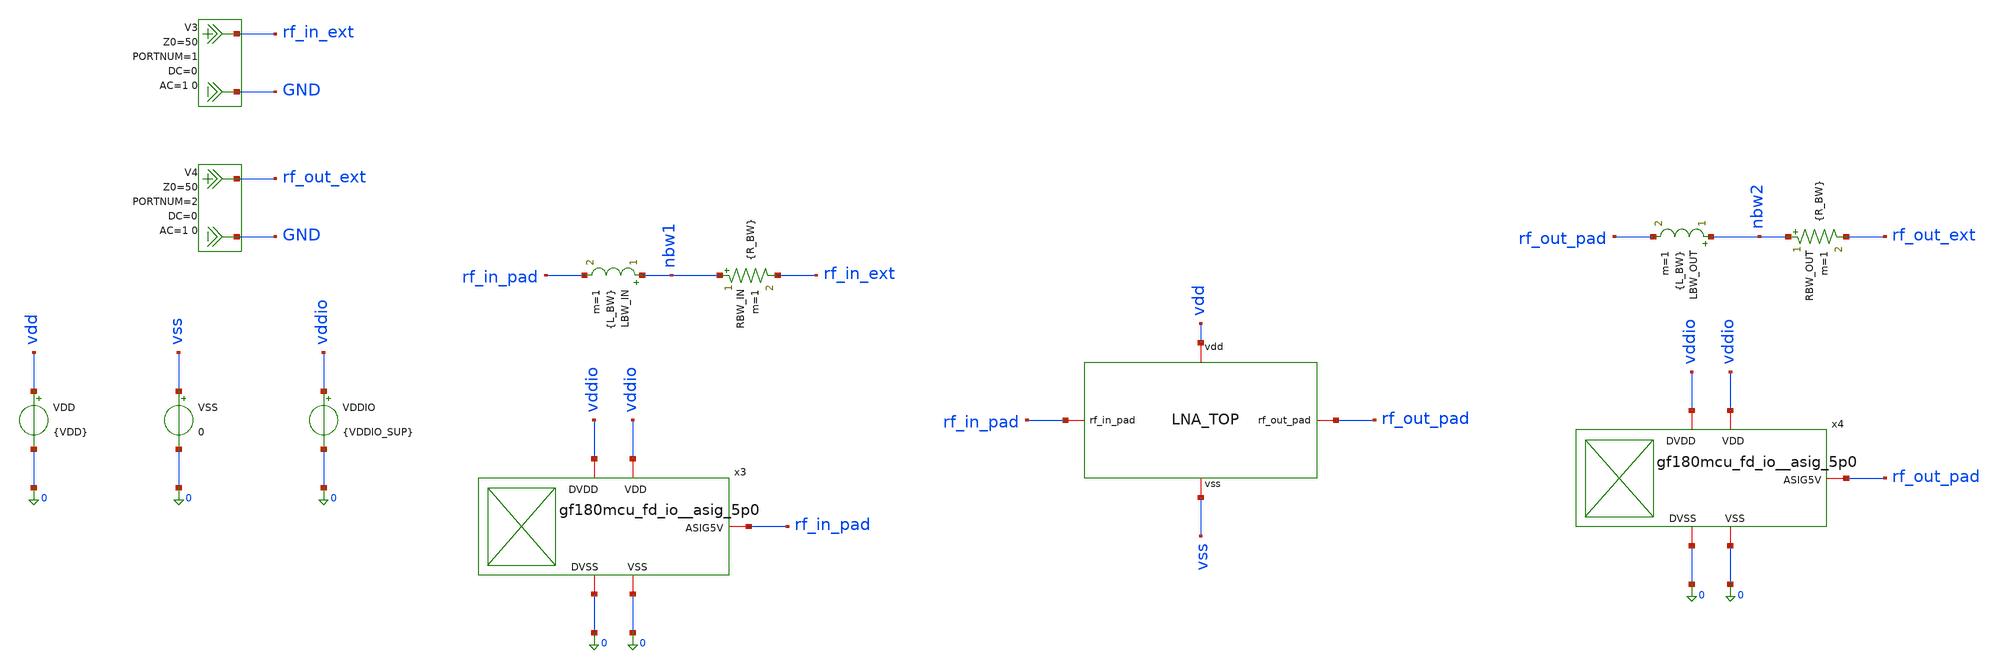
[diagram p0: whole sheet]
** sch_path: xschem/lna_v2/lna_top_tb.sch
**.subckt lna_top_tb
x3 rf_in_pad vddio 0 vddio 0 gf180mcu_fd_io__asig_5p0
x4 rf_out_pad vddio 0 vddio 0 gf180mcu_fd_io__asig_5p0
LBW_IN nbw1 rf_in_pad {L_BW} m=1
RBW_IN nbw1 rf_in_ext {R_BW} m=1
LBW_OUT nbw2 rf_out_pad {L_BW} m=1
RBW_OUT nbw2 rf_out_ext {R_BW} m=1
VDD vdd 0 {VDD}
VSS vss 0 0
VDDIO vddio 0 {VDDIO_SUP}
V3 rf_in_ext GND DC 0 AC 1 0 portnum 1 z0 50
V4 rf_out_ext GND DC 0 AC 1 0 portnum 2 z0 50
x1 vdd rf_in_pad rf_out_pad vss lna_top
**** begin user architecture code

.include ${::180MCU_MODELS}/design.ngspice
.lib ${::180MCU_MODELS}/sm141064.ngspice typical
.lib ${::180MCU_MODELS}/sm141064.ngspice res_typical
.lib ${::180MCU_MODELS}/sm141064.ngspice moscap_typical
.lib ${::180MCU_MODELS}/sm141064.ngspice diode_typical
.lib ${::180MCU_MODELS}/sm141064.ngspice bjt_typical
.lib ${::180MCU_MODELS}/sm141064.ngspice mimcap_typical



* extracted RC pad network (magic flat RC extraction, nominal); high-C corner: pad_rcxhrhc.spice
*.include /home/arjun/.xschem/simulations/lna_test/optimization/pad_audit/pad_rcxnom.spice
.include /home/arjun/eda/projects/The-Silent-Owl-GF180MCU-WB-LNA/analog_pad_sp_paramerters/spice_files/extracted_gf180mcu_fd_io__asig_5p0_manually_scaled.spice




.param VDD=5.0 VDDIO_SUP=5.0 L_BW=3n R_BW=0.2
.temp 27





.control

set noaskquit
set wr_singlescale
set wr_vecnames
set numdgt=10

option klu
set num_threads=6

let spec_gain_min_db = 10
let spec_s11_max_db  = -10
let spec_s22_max_db  = -10
let spec_nf_max_db   = 2.0
let spec_mu_min      = 1.0
let spec_k_min       = 1.0
let spec_delta_max   = 1.0
let spec_pdc_max_mw  = 130

let f_target_lo = 2.3e9
let f_target    = 2.4e9
let f_target_hi = 2.5e9



echo ============================================================ > lna_final_report.txt
echo GF180MCU_WIDEBAND_LNA_FINAL_CHARACTERIZATION >> lna_final_report.txt
echo ============================================================ >> lna_final_report.txt
echo TARGET_CENTER_HZ 2.400e9 >> lna_final_report.txt
echo TARGET_BAND_HZ 2.300e9 2.500e9 >> lna_final_report.txt
echo PORT_REFERENCE_OHM 50 >> lna_final_report.txt
echo VDD_NOMINAL_V 5.0 >> lna_final_report.txt
echo HIERARCHY TB_X1_LNA_TOP_X1_LNA_CORE >> lna_final_report.txt
echo S_PARAMETER_REFERENCE_PLANE EXTERNAL_PORTS_INCLUDING_PADS_BONDWIRES >> lna_final_report.txt

echo SPEC_GAIN_MIN_DB $&spec_gain_min_db >> lna_final_report.txt
echo SPEC_S11_MAX_DB $&spec_s11_max_db >> lna_final_report.txt
echo SPEC_S22_MAX_DB $&spec_s22_max_db >> lna_final_report.txt
echo SPEC_NF_MAX_DB $&spec_nf_max_db >> lna_final_report.txt
echo SPEC_PDC_MAX_MW $&spec_pdc_max_mw >> lna_final_report.txt
echo ============================================================ >> lna_final_report.txt


op


let pdc_lna_mw = 1e3*abs(i(VDD))*v(vdd)
let pdc_io_mw  = 1e3*abs(i(VDDIO))*v(vddio)
let pdc_total_mw = pdc_lna_mw+pdc_io_mw

let idd_lna = abs(i(VDD))
let idd_io  = abs(i(VDDIO))

set op_pdc_lna   = $&pdc_lna_mw
set op_pdc_io    = $&pdc_io_mw
set op_pdc_total = $&pdc_total_mw
set op_idd_lna   = $&idd_lna
set op_idd_io    = $&idd_io



let vbias_cg_op   = v(x1.vbias_cg)
let vbias_cs_op   = v(x1.vbias_cs)
let vbias_csc_op  = v(x1.vbias_csc)
let vbias_cas_op  = v(x1.vbias_cas)
let vbias_casc_op = v(x1.vbias_casc)

set op_vbias_cg   = $&vbias_cg_op
set op_vbias_cs   = $&vbias_cs_op
set op_vbias_csc  = $&vbias_csc_op
set op_vbias_cas  = $&vbias_cas_op
set op_vbias_casc = $&vbias_casc_op


let vm2_op     = v(x1.x1.vm2)
let gcg_op     = v(x1.x1.g_cg)

let gcs_op     = v(x1.x1.g_cs)
let xm1s_op    = v(x1.x1.xm1_s)
let vm1_op     = v(x1.x1.vm1)

let gcsc_op    = v(x1.x1.g_csc)
let xm9s_op    = v(x1.x1.xm9_s)
let xm9d_op    = v(x1.x1.xm9_d)

let vx_op      = v(x1.x1.vx)

let vbp3_op    = v(x1.x1.vbp3)
let ngp3_op    = v(x1.x1.ngp3)
let np3d_op    = v(x1.x1.np3d)
let noutc_op   = v(x1.x1.nout_c)

set op_vm2   = $&vm2_op
set op_gcg   = $&gcg_op
set op_gcs   = $&gcs_op
set op_xm1s  = $&xm1s_op
set op_vm1   = $&vm1_op
set op_gcsc  = $&gcsc_op
set op_xm9s  = $&xm9s_op
set op_xm9d  = $&xm9d_op
set op_vx    = $&vx_op
set op_vbp3  = $&vbp3_op
set op_ngp3  = $&ngp3_op
set op_np3d  = $&np3d_op
set op_noutc = $&noutc_op

let id1    = abs(@m.x1.x1.xm1.m0[id])
let gm1    = abs(@m.x1.x1.xm1.m0[gm])
let gmb1   = abs(@m.x1.x1.xm1.m0[gmbs])
let gds1   = abs(@m.x1.x1.xm1.m0[gds])

let vgs1   = @m.x1.x1.xm1.m0[vgs]
let vds1   = @m.x1.x1.xm1.m0[vds]
let vth1   = @m.x1.x1.xm1.m0[vth]
let vdsat1 = @m.x1.x1.xm1.m0[vdsat]

let gmid1  = gm1/(id1+1e-30)
let ro1    = 1/(gds1+1e-30)
let sat1   = abs(vds1)-abs(vdsat1)

let id2    = abs(@m.x1.x1.xm2.m0[id])
let gm2    = abs(@m.x1.x1.xm2.m0[gm])
let gmb2   = abs(@m.x1.x1.xm2.m0[gmbs])
let gds2   = abs(@m.x1.x1.xm2.m0[gds])

let vgs2   = @m.x1.x1.xm2.m0[vgs]
let vds2   = @m.x1.x1.xm2.m0[vds]
let vth2   = @m.x1.x1.xm2.m0[vth]
let vdsat2 = @m.x1.x1.xm2.m0[vdsat]

let gmid2  = gm2/(id2+1e-30)
let ro2    = 1/(gds2+1e-30)
let sat2   = abs(vds2)-abs(vdsat2)

let id4    = abs(@m.x1.x1.xm4.m0[id])
let gm4    = abs(@m.x1.x1.xm4.m0[gm])
let gmb4   = abs(@m.x1.x1.xm4.m0[gmbs])
let gds4   = abs(@m.x1.x1.xm4.m0[gds])

let vgs4   = @m.x1.x1.xm4.m0[vgs]
let vds4   = @m.x1.x1.xm4.m0[vds]
let vth4   = @m.x1.x1.xm4.m0[vth]
let vdsat4 = @m.x1.x1.xm4.m0[vdsat]

let gmid4  = gm4/(id4+1e-30)
let ro4    = 1/(gds4+1e-30)
let sat4   = abs(vds4)-abs(vdsat4)

let id9    = abs(@m.x1.x1.xm9.m0[id])
let gm9    = abs(@m.x1.x1.xm9.m0[gm])
let gmb9   = abs(@m.x1.x1.xm9.m0[gmbs])
let gds9   = abs(@m.x1.x1.xm9.m0[gds])

let vgs9   = @m.x1.x1.xm9.m0[vgs]
let vds9   = @m.x1.x1.xm9.m0[vds]
let vth9   = @m.x1.x1.xm9.m0[vth]
let vdsat9 = @m.x1.x1.xm9.m0[vdsat]

let gmid9  = gm9/(id9+1e-30)
let ro9    = 1/(gds9+1e-30)
let sat9   = abs(vds9)-abs(vdsat9)

let id7    = abs(@m.x1.x1.xm7.m0[id])
let gm7    = abs(@m.x1.x1.xm7.m0[gm])
let gmb7   = abs(@m.x1.x1.xm7.m0[gmbs])
let gds7   = abs(@m.x1.x1.xm7.m0[gds])

let vgs7   = @m.x1.x1.xm7.m0[vgs]
let vds7   = @m.x1.x1.xm7.m0[vds]
let vth7   = @m.x1.x1.xm7.m0[vth]
let vdsat7 = @m.x1.x1.xm7.m0[vdsat]

let gmid7  = gm7/(id7+1e-30)
let ro7    = 1/(gds7+1e-30)
let sat7   = abs(vds7)-abs(vdsat7)

let idp3    = abs(@m.x1.x1.xmp3.m0[id])
let gmp3    = abs(@m.x1.x1.xmp3.m0[gm])
let gmbp3   = abs(@m.x1.x1.xmp3.m0[gmbs])
let gdsp3   = abs(@m.x1.x1.xmp3.m0[gds])

let vgsp3   = @m.x1.x1.xmp3.m0[vgs]
let vdsp3   = @m.x1.x1.xmp3.m0[vds]
let vthp3   = @m.x1.x1.xmp3.m0[vth]
let vdsatp3 = @m.x1.x1.xmp3.m0[vdsat]

let gmidp3  = gmp3/(idp3+1e-30)
let rop3    = 1/(gdsp3+1e-30)
let satp3   = abs(vdsp3)-abs(vdsatp3)


let idbp3    = abs(@m.x1.x1.xbp3.m0[id])
let gmbp3x   = abs(@m.x1.x1.xbp3.m0[gm])
let gdsbp3   = abs(@m.x1.x1.xbp3.m0[gds])

let vgsbp3   = @m.x1.x1.xbp3.m0[vgs]
let vdsbp3   = @m.x1.x1.xbp3.m0[vds]
let vthbp3   = @m.x1.x1.xbp3.m0[vth]
let vdsatbp3 = @m.x1.x1.xbp3.m0[vdsat]

let gmidbp3 = gmbp3x/(idbp3+1e-30)
let robp3   = 1/(gdsbp3+1e-30)
let satbp3  = abs(vdsbp3)-abs(vdsatbp3)

set op_id1=$&id1
set op_gm1=$&gm1
set op_gmid1=$&gmid1
set op_ro1=$&ro1
set op_vgs1=$&vgs1
set op_vds1=$&vds1
set op_vdsat1=$&vdsat1
set op_sat1=$&sat1

set op_id2=$&id2
set op_gm2=$&gm2
set op_gmid2=$&gmid2
set op_ro2=$&ro2
set op_vgs2=$&vgs2
set op_vds2=$&vds2
set op_vdsat2=$&vdsat2
set op_sat2=$&sat2

set op_id4=$&id4
set op_gm4=$&gm4
set op_gmid4=$&gmid4
set op_ro4=$&ro4
set op_vgs4=$&vgs4
set op_vds4=$&vds4
set op_vdsat4=$&vdsat4
set op_sat4=$&sat4

set op_id9=$&id9
set op_gm9=$&gm9
set op_gmid9=$&gmid9
set op_ro9=$&ro9
set op_vgs9=$&vgs9
set op_vds9=$&vds9
set op_vdsat9=$&vdsat9
set op_sat9=$&sat9

set op_id7=$&id7
set op_gm7=$&gm7
set op_gmid7=$&gmid7
set op_ro7=$&ro7
set op_vgs7=$&vgs7
set op_vds7=$&vds7
set op_vdsat7=$&vdsat7
set op_sat7=$&sat7

set op_idp3=$&idp3
set op_gmp3=$&gmp3
set op_gmidp3=$&gmidp3
set op_rop3=$&rop3
set op_vgsp3=$&vgsp3
set op_vdsp3=$&vdsp3
set op_vdsatp3=$&vdsatp3
set op_satp3=$&satp3

set op_idbp3=$&idbp3
set op_gmbp3=$&gmbp3x
set op_gmidbp3=$&gmidbp3
set op_robp3=$&robp3
set op_vgsbp3=$&vgsbp3
set op_vdsbp3=$&vdsbp3
set op_vdsatbp3=$&vdsatbp3
set op_satbp3=$&satbp3


* ============================================================================
* WRITE DC REPORT
* ============================================================================

echo ============================================================ >> lna_final_report.txt
echo DC_POWER >> lna_final_report.txt
echo ============================================================ >> lna_final_report.txt

echo LNA_TOP_POWER_MW $op_pdc_lna >> lna_final_report.txt
echo IO_PAD_POWER_MW $op_pdc_io >> lna_final_report.txt
echo TOTAL_POWER_MW $op_pdc_total >> lna_final_report.txt
echo LNA_TOP_CURRENT_A $op_idd_lna >> lna_final_report.txt
echo IO_CURRENT_A $op_idd_io >> lna_final_report.txt


echo ============================================================ >> lna_final_report.txt
echo BIAS_VOLTAGES >> lna_final_report.txt
echo ============================================================ >> lna_final_report.txt

echo VBIAS_CG_V $op_vbias_cg >> lna_final_report.txt
echo VBIAS_CS_V $op_vbias_cs >> lna_final_report.txt
echo VBIAS_CSC_V $op_vbias_csc >> lna_final_report.txt
echo VBIAS_CAS_V $op_vbias_cas >> lna_final_report.txt
echo VBIAS_CASC_V $op_vbias_casc >> lna_final_report.txt


echo ============================================================ >> lna_final_report.txt
echo CORE_DC_NODE_VOLTAGES >> lna_final_report.txt
echo ============================================================ >> lna_final_report.txt

echo VM2_V $op_vm2 >> lna_final_report.txt
echo G_CG_V $op_gcg >> lna_final_report.txt

echo G_CS_V $op_gcs >> lna_final_report.txt
echo XM1_SOURCE_V $op_xm1s >> lna_final_report.txt
echo VM1_V $op_vm1 >> lna_final_report.txt

echo G_CSC_V $op_gcsc >> lna_final_report.txt
echo XM9_SOURCE_V $op_xm9s >> lna_final_report.txt
echo XM9_DRAIN_V $op_xm9d >> lna_final_report.txt

echo VX_V $op_vx >> lna_final_report.txt

echo VBP3_V $op_vbp3 >> lna_final_report.txt
echo NGP3_V $op_ngp3 >> lna_final_report.txt
echo NP3D_V $op_np3d >> lna_final_report.txt
echo NOUT_C_V $op_noutc >> lna_final_report.txt


echo ============================================================ >> lna_final_report.txt
echo TRANSISTOR_OPERATING_POINTS >> lna_final_report.txt
echo FIELDS ID_A GM_S GMID_1_PER_V RO_OHM VGS_V VDS_V VDSAT_V SAT_MARGIN_V >> lna_final_report.txt
echo ============================================================ >> lna_final_report.txt

echo XM1_MAIN_CS ID $op_id1 GM $op_gm1 GMID $op_gmid1 RO $op_ro1 VGS $op_vgs1 VDS $op_vds1 VDSAT
+ $op_vdsat1 SAT_MARGIN $op_sat1 >> lna_final_report.txt

echo XM2_INPUT_CG ID $op_id2 GM $op_gm2 GMID $op_gmid2 RO $op_ro2 VGS $op_vgs2 VDS $op_vds2 VDSAT
+ $op_vdsat2 SAT_MARGIN $op_sat2 >> lna_final_report.txt

echo XM4_MAIN_CASCODE ID $op_id4 GM $op_gm4 GMID $op_gmid4 RO $op_ro4 VGS $op_vgs4 VDS $op_vds4
+ VDSAT $op_vdsat4 SAT_MARGIN $op_sat4 >> lna_final_report.txt

echo XM9_CANCELLATION_CS ID $op_id9 GM $op_gm9 GMID $op_gmid9 RO $op_ro9 VGS $op_vgs9 VDS $op_vds9
+ VDSAT $op_vdsat9 SAT_MARGIN $op_sat9 >> lna_final_report.txt

echo XM7_CANCELLATION_CASCODE ID $op_id7 GM $op_gm7 GMID $op_gmid7 RO $op_ro7 VGS $op_vgs7 VDS
+ $op_vds7 VDSAT $op_vdsat7 SAT_MARGIN $op_sat7 >> lna_final_report.txt

echo XMP3_OUTPUT_PMOS ID $op_idp3 GM $op_gmp3 GMID $op_gmidp3 RO $op_rop3 VGS $op_vgsp3 VDS
+ $op_vdsp3 VDSAT $op_vdsatp3 SAT_MARGIN $op_satp3 >> lna_final_report.txt

echo XBP3_PMOS_BIAS ID $op_idbp3 GM $op_gmbp3 GMID $op_gmidbp3 RO $op_robp3 VGS $op_vgsbp3 VDS
+ $op_vdsbp3 VDSAT $op_vdsatbp3 SAT_MARGIN $op_satbp3 >> lna_final_report.txt


* ============================================================================
* POWER SPECIFICATION CHECK
* ============================================================================

echo ============================================================ >> lna_final_report.txt
echo DC_SPEC_CHECK >> lna_final_report.txt

if pdc_lna_mw <= spec_pdc_max_mw
    echo POWER PASS >> lna_final_report.txt
else
    echo POWER FAIL >> lna_final_report.txt
end


* We no longer require OP plot vectors after storing scalar values.
destroy $curplot



* ============================================================================
* 2. BROADBAND S-PARAMETER + NOISE ANALYSIS
*
* SP noise flag = 1.
*
* 7000 linearly spaced points:
*   1 MHz --> 7 GHz
*
* This gives roughly 1 MHz resolution, including the complete 2.3-2.5 GHz
* target band.
* ============================================================================

reset
sp lin 7000 1Meg 7Gig 1

set rfplot=$curplot

let fghz=frequency/1e9


* ============================================================================
* S PARAMETERS
* ============================================================================

let s11db=db(s_1_1)
let s21db=db(s_2_1)
let s12db=db(s_1_2)
let s22db=db(s_2_2)

let a11=mag(s_1_1)
let a21=mag(s_2_1)
let a12=mag(s_1_2)
let a22=mag(s_2_2)


* ============================================================================
* NOISE
* ============================================================================

let nfdb=real(NF)
let nfmin_db=real(NFmin)


* ============================================================================
* STABILITY FROM S-PARAMETERS
* ============================================================================

let delta=s_1_1*s_2_2-s_1_2*s_2_1
let delta_mag=mag(delta)

let kval=(1-a11*a11-a22*a22+delta_mag*delta_mag)/(2*a12*a21+1e-30)

let mu=(1-a11*a11)/(mag(s_2_2-delta*conj(s_1_1))+mag(s_1_2*s_2_1)+1e-30)

let mup=(1-a22*a22)/(mag(s_1_1-delta*conj(s_2_2))+mag(s_1_2*s_2_1)+1e-30)


* ============================================================================
* INPUT / OUTPUT IMPEDANCE
* ============================================================================

let zin=50*(1+s_1_1)/(1-s_1_1)
let zout=50*(1+s_2_2)/(1-s_2_2)

let zin_re=real(zin)
let zin_im=imag(zin)

let zout_re=real(zout)
let zout_im=imag(zout)


* ============================================================================
* INPUT / OUTPUT VSWR
* ============================================================================

let vswr_in=(1+a11)/(1-a11+1e-30)
let vswr_out=(1+a22)/(1-a22+1e-30)


* ============================================================================
* FIND 2.3 / 2.4 / 2.5 GHz INDICES
* ============================================================================

let npts=length(frequency)

let ilo=0
let icenter=0
let ihi=0

let errlo=abs(frequency[0]-2.3e9)
let errcenter=abs(frequency[0]-2.4e9)
let errhi=abs(frequency[0]-2.5e9)

let ii=1

while ii < npts

    let newerr=abs(frequency[ii]-2.3e9)

    if newerr < errlo
        let errlo=newerr
        let ilo=ii
    end

    let newerr=abs(frequency[ii]-2.4e9)

    if newerr < errcenter
        let errcenter=newerr
        let icenter=ii
    end

    let newerr=abs(frequency[ii]-2.5e9)

    if newerr < errhi
        let errhi=newerr
        let ihi=ii
    end

    let ii=ii+1

end


* ============================================================================
* VALUES AT 2.4 GHz
* ============================================================================

let fc=frequency[icenter]

let s11c=s11db[icenter]
let s21c=s21db[icenter]
let s12c=s12db[icenter]
let s22c=s22db[icenter]

let nfc=nfdb[icenter]
let nfminc=nfmin_db[icenter]

let kc=kval[icenter]
let muc=mu[icenter]
let mupc=mup[icenter]
let deltac=delta_mag[icenter]

let zinrc=zin_re[icenter]
let zinic=zin_im[icenter]

let zoutrc=zout_re[icenter]
let zoutic=zout_im[icenter]

let vswrinc=vswr_in[icenter]
let vswroutc=vswr_out[icenter]


* ============================================================================
* TARGET-BAND MIN / MAX INITIALIZATION
* ============================================================================

let s11min=s11db[ilo]
let s11max=s11db[ilo]

let s21min=s21db[ilo]
let s21max=s21db[ilo]

let s12min=s12db[ilo]
let s12max=s12db[ilo]

let s22min=s22db[ilo]
let s22max=s22db[ilo]

let nfbandmin=nfdb[ilo]
let nfbandmax=nfdb[ilo]

let nfminpar_min=nfmin_db[ilo]
let nfminpar_max=nfmin_db[ilo]

let kbandmin=kval[ilo]
let mubandmin=mu[ilo]
let mupbandmin=mup[ilo]

let deltabandmax=delta_mag[ilo]

let zinremin=zin_re[ilo]
let zinremax=zin_re[ilo]

let vswrinmax=vswr_in[ilo]
let vswroutmax=vswr_out[ilo]


* indices
let s11max_i=ilo
let s21min_i=ilo
let s21max_i=ilo
let s22max_i=ilo

let nfmax_i=ilo
let nfmin_i=ilo

let kmin_i=ilo
let mumin_i=ilo
let mupmin_i=ilo
let deltamax_i=ilo

let vswrinmax_i=ilo
let vswroutmax_i=ilo


* ============================================================================
* TARGET-BAND SEARCH
* ============================================================================

let ii=ilo

while ii <= ihi

    if s11db[ii] < s11min
        let s11min=s11db[ii]
    end

    if s11db[ii] > s11max
        let s11max=s11db[ii]
        let s11max_i=ii
    end


    if s21db[ii] < s21min
        let s21min=s21db[ii]
        let s21min_i=ii
    end

    if s21db[ii] > s21max
        let s21max=s21db[ii]
        let s21max_i=ii
    end


    if s12db[ii] < s12min
        let s12min=s12db[ii]
    end

    if s12db[ii] > s12max
        let s12max=s12db[ii]
    end


    if s22db[ii] < s22min
        let s22min=s22db[ii]
    end

    if s22db[ii] > s22max
        let s22max=s22db[ii]
        let s22max_i=ii
    end


    if nfdb[ii] < nfbandmin
        let nfbandmin=nfdb[ii]
        let nfmin_i=ii
    end

    if nfdb[ii] > nfbandmax
        let nfbandmax=nfdb[ii]
        let nfmax_i=ii
    end


    if nfmin_db[ii] < nfminpar_min
        let nfminpar_min=nfmin_db[ii]
    end

    if nfmin_db[ii] > nfminpar_max
        let nfminpar_max=nfmin_db[ii]
    end


    if kval[ii] < kbandmin
        let kbandmin=kval[ii]
        let kmin_i=ii
    end

    if mu[ii] < mubandmin
        let mubandmin=mu[ii]
        let mumin_i=ii
    end

    if mup[ii] < mupbandmin
        let mupbandmin=mup[ii]
        let mupmin_i=ii
    end

    if delta_mag[ii] > deltabandmax
        let deltabandmax=delta_mag[ii]
        let deltamax_i=ii
    end


    if vswr_in[ii] > vswrinmax
        let vswrinmax=vswr_in[ii]
        let vswrinmax_i=ii
    end

    if vswr_out[ii] > vswroutmax
        let vswroutmax=vswr_out[ii]
        let vswroutmax_i=ii
    end

    let ii=ii+1

end


* ============================================================================
* DERIVED BAND METRICS
* ============================================================================

let gain_ripple=s21max-s21min

let s11worst_f=frequency[s11max_i]
let s21min_f=frequency[s21min_i]
let s21max_f=frequency[s21max_i]
let s22worst_f=frequency[s22max_i]

let nfmin_f=frequency[nfmin_i]
let nfmax_f=frequency[nfmax_i]

let kmin_f=frequency[kmin_i]
let mumin_f=frequency[mumin_i]
let mupmin_f=frequency[mupmin_i]
let deltamax_f=frequency[deltamax_i]

let vswrinmax_f=frequency[vswrinmax_i]
let vswroutmax_f=frequency[vswroutmax_i]


* ============================================================================
* BROADBAND GAIN PEAK
* ============================================================================

let imax=0
let gainmax=s21db[0]

let ii=1

while ii < npts

    if s21db[ii] > gainmax
        let gainmax=s21db[ii]
        let imax=ii
    end

    let ii=ii+1

end

let peakfreq=frequency[imax]


* ============================================================================
* TARGET-CENTERED 10-dB GAIN BANDWIDTH
* ============================================================================

let bw_valid=0
let bwflo=0
let bwfhi=0
let bwval=0
let bwcenter=0
let bwfbw=0

if s21c >= spec_gain_min_db

    let bwlo=icenter
    let bwhi=icenter

    let searching=1

    while searching = 1

        if bwlo > 0

            if s21db[bwlo-1] >= spec_gain_min_db
                let bwlo=bwlo-1
            else
                let searching=0
            end

        else
            let searching=0
        end

    end


    let searching=1

    while searching = 1

        if bwhi < npts-1

            if s21db[bwhi+1] >= spec_gain_min_db
                let bwhi=bwhi+1
            else
                let searching=0
            end

        else
            let searching=0
        end

    end


    let bwflo=frequency[bwlo]
    let bwfhi=frequency[bwhi]

    let bwval=bwfhi-bwflo

    let bwcenter=0.5*(bwfhi+bwflo)

    let bwfbw=100*bwval/(bwcenter+1e-30)

    let bw_valid=1

end


* ============================================================================
* RF REPORT
* ============================================================================

echo ============================================================ >> lna_final_report.txt
echo RF_AT_2P4_GHZ >> lna_final_report.txt
echo ============================================================ >> lna_final_report.txt

echo ACTUAL_SAMPLE_HZ $&fc >> lna_final_report.txt

echo S11_DB $&s11c >> lna_final_report.txt
echo S21_DB $&s21c >> lna_final_report.txt
echo S12_DB $&s12c >> lna_final_report.txt
echo S22_DB $&s22c >> lna_final_report.txt

echo NF_DB $&nfc >> lna_final_report.txt
echo NFMIN_DB $&nfminc >> lna_final_report.txt

echo K $&kc >> lna_final_report.txt
echo MU $&muc >> lna_final_report.txt
echo MUP $&mupc >> lna_final_report.txt
echo DELTA_MAG $&deltac >> lna_final_report.txt

echo ZIN_OHM_REAL $&zinrc IMAG $&zinic >> lna_final_report.txt
echo ZOUT_OHM_REAL $&zoutrc IMAG $&zoutic >> lna_final_report.txt

echo VSWR_IN $&vswrinc >> lna_final_report.txt
echo VSWR_OUT $&vswroutc >> lna_final_report.txt


echo ============================================================ >> lna_final_report.txt
echo TARGET_BAND_2P3_TO_2P5_GHZ >> lna_final_report.txt
echo ============================================================ >> lna_final_report.txt

echo S11_BEST_DB $&s11min >> lna_final_report.txt
echo S11_WORST_DB $&s11max AT_HZ $&s11worst_f >> lna_final_report.txt

echo S21_MIN_DB $&s21min AT_HZ $&s21min_f >> lna_final_report.txt
echo S21_MAX_DB $&s21max AT_HZ $&s21max_f >> lna_final_report.txt
echo S21_RIPPLE_DB $&gain_ripple >> lna_final_report.txt

echo S12_MIN_DB $&s12min >> lna_final_report.txt
echo S12_MAX_DB $&s12max >> lna_final_report.txt

echo S22_BEST_DB $&s22min >> lna_final_report.txt
echo S22_WORST_DB $&s22max AT_HZ $&s22worst_f >> lna_final_report.txt

echo NF_MIN_DB $&nfbandmin AT_HZ $&nfmin_f >> lna_final_report.txt
echo NF_MAX_DB $&nfbandmax AT_HZ $&nfmax_f >> lna_final_report.txt

echo NFMIN_PARAMETER_MIN_DB $&nfminpar_min >> lna_final_report.txt
echo NFMIN_PARAMETER_MAX_DB $&nfminpar_max >> lna_final_report.txt

echo K_MIN $&kbandmin AT_HZ $&kmin_f >> lna_final_report.txt
echo MU_MIN $&mubandmin AT_HZ $&mumin_f >> lna_final_report.txt
echo MUP_MIN $&mupbandmin AT_HZ $&mupmin_f >> lna_final_report.txt
echo DELTA_MAX $&deltabandmax AT_HZ $&deltamax_f >> lna_final_report.txt

echo VSWR_IN_MAX $&vswrinmax AT_HZ $&vswrinmax_f >> lna_final_report.txt
echo VSWR_OUT_MAX $&vswroutmax AT_HZ $&vswroutmax_f >> lna_final_report.txt


echo ============================================================ >> lna_final_report.txt
echo BROADBAND_GAIN >> lna_final_report.txt
echo ============================================================ >> lna_final_report.txt

echo PEAK_GAIN_DB $&gainmax >> lna_final_report.txt
echo PEAK_GAIN_FREQUENCY_HZ $&peakfreq >> lna_final_report.txt


echo ============================================================ >> lna_final_report.txt
echo TARGET_CENTERED_GAIN_BANDWIDTH >> lna_final_report.txt
echo ============================================================ >> lna_final_report.txt

if bw_valid = 1

    echo LOWER_HZ $&bwflo >> lna_final_report.txt
    echo UPPER_HZ $&bwfhi >> lna_final_report.txt
    echo BANDWIDTH_HZ $&bwval >> lna_final_report.txt
    echo BAND_CENTER_HZ $&bwcenter >> lna_final_report.txt
    echo FRACTIONAL_BW_PERCENT $&bwfbw >> lna_final_report.txt

else

    echo NO_CONTIGUOUS_TARGET_CENTERED_GAIN_BAND >> lna_final_report.txt

end


* ============================================================================
* TARGET-BAND PASS / FAIL
* ============================================================================

echo ============================================================ >> lna_final_report.txt
echo TARGET_BAND_SPECIFICATION_CHECK >> lna_final_report.txt
echo ============================================================ >> lna_final_report.txt


if s21min >= spec_gain_min_db
    echo GAIN PASS >> lna_final_report.txt
else
    echo GAIN FAIL >> lna_final_report.txt
end


if s11max <= spec_s11_max_db
    echo INPUT_MATCH_S11 PASS >> lna_final_report.txt
else
    echo INPUT_MATCH_S11 FAIL >> lna_final_report.txt
end


if s22max <= spec_s22_max_db
    echo OUTPUT_MATCH_S22 PASS >> lna_final_report.txt
else
    echo OUTPUT_MATCH_S22 FAIL >> lna_final_report.txt
end


if nfbandmax <= spec_nf_max_db
    echo NOISE_FIGURE PASS >> lna_final_report.txt
else
    echo NOISE_FIGURE FAIL >> lna_final_report.txt
end


if mubandmin > spec_mu_min

    if mupbandmin > spec_mu_min
        echo MU_STABILITY_TARGET_BAND PASS >> lna_final_report.txt
    else
        echo MU_STABILITY_TARGET_BAND FAIL >> lna_final_report.txt
    end

else

    echo MU_STABILITY_TARGET_BAND FAIL >> lna_final_report.txt

end


if kbandmin > spec_k_min

    if deltabandmax < spec_delta_max
        echo ROLLETT_K_DELTA_TARGET_BAND PASS >> lna_final_report.txt
    else
        echo ROLLETT_K_DELTA_TARGET_BAND FAIL >> lna_final_report.txt
    end

else

    echo ROLLETT_K_DELTA_TARGET_BAND FAIL >> lna_final_report.txt

end


* ============================================================================
* SAVE RF DATA
* ============================================================================

wrdata lna_final_target_and_broadband.dat frequency s11db s21db s12db s22db nfdb nfmin_db kval mu
+ mup delta_mag zin_re zin_im zout_re zout_im vswr_in vswr_out

write lna_final_rf.raw


* ============================================================================
* 3. VERY-WIDEBAND STABILITY ANALYSIS
*
* Deliberately much wider than operating band.
* No noise calculation required here.
* ============================================================================

reset
sp dec 101 10Meg 30Gig 0

set stabilityplot=$curplot

let wbfghz=frequency/1e9

let wba11=mag(s_1_1)
let wba21=mag(s_2_1)
let wba12=mag(s_1_2)
let wba22=mag(s_2_2)

let wbdelta=s_1_1*s_2_2-s_1_2*s_2_1
let wbdelta_mag=mag(wbdelta)

let wbk=(1-wba11*wba11-wba22*wba22+wbdelta_mag*wbdelta_mag)/(2*wba12*wba21+1e-30)

let wbmu=(1-wba11*wba11)/(mag(s_2_2-wbdelta*conj(s_1_1))+mag(s_1_2*s_2_1)+1e-30)

let wbmup=(1-wba22*wba22)/(mag(s_1_1-wbdelta*conj(s_2_2))+mag(s_1_2*s_2_1)+1e-30)


* ============================================================================
* SEARCH WIDEBAND WORST-CASE STABILITY + FREQUENCIES
* ============================================================================

let wbnpts=length(frequency)

let wbkmin=wbk[0]
let wbmumin=wbmu[0]
let wbmupmin=wbmup[0]
let wbdeltamax=wbdelta_mag[0]

let wbkmin_i=0
let wbmumin_i=0
let wbmupmin_i=0
let wbdeltamax_i=0

let ii=1

while ii < wbnpts

    if wbk[ii] < wbkmin
        let wbkmin=wbk[ii]
        let wbkmin_i=ii
    end

    if wbmu[ii] < wbmumin
        let wbmumin=wbmu[ii]
        let wbmumin_i=ii
    end

    if wbmup[ii] < wbmupmin
        let wbmupmin=wbmup[ii]
        let wbmupmin_i=ii
    end

    if wbdelta_mag[ii] > wbdeltamax
        let wbdeltamax=wbdelta_mag[ii]
        let wbdeltamax_i=ii
    end

    let ii=ii+1

end

let wbkmin_f=frequency[wbkmin_i]
let wbmumin_f=frequency[wbmumin_i]
let wbmupmin_f=frequency[wbmupmin_i]
let wbdeltamax_f=frequency[wbdeltamax_i]


echo ============================================================ >> lna_final_report.txt
echo WIDEBAND_STABILITY_10MHZ_TO_30GHZ >> lna_final_report.txt
echo ============================================================ >> lna_final_report.txt

echo K_MIN $&wbkmin AT_HZ $&wbkmin_f >> lna_final_report.txt
echo MU_MIN $&wbmumin AT_HZ $&wbmumin_f >> lna_final_report.txt
echo MUP_MIN $&wbmupmin AT_HZ $&wbmupmin_f >> lna_final_report.txt
echo DELTA_MAX $&wbdeltamax AT_HZ $&wbdeltamax_f >> lna_final_report.txt


* ============================================================================
* WIDEBAND STABILITY PASS / FAIL
*
* μ and μ' > 1 across entire range is the preferred robust test.
* K > 1 and |Delta| < 1 is also reported.
* ============================================================================

if wbmumin > 1

    if wbmupmin > 1
        echo WIDEBAND_MU_STABILITY PASS >> lna_final_report.txt
    else
        echo WIDEBAND_MU_STABILITY FAIL >> lna_final_report.txt
    end

else

    echo WIDEBAND_MU_STABILITY FAIL >> lna_final_report.txt

end


if wbkmin > 1

    if wbdeltamax < 1
        echo WIDEBAND_K_DELTA_STABILITY PASS >> lna_final_report.txt
    else
        echo WIDEBAND_K_DELTA_STABILITY FAIL >> lna_final_report.txt
    end

else

    echo WIDEBAND_K_DELTA_STABILITY FAIL >> lna_final_report.txt

end


wrdata lna_final_stability.dat frequency wbk wbmu wbmup wbdelta_mag

write lna_final_stability.raw


* ============================================================================
* FINAL SUMMARY
* ============================================================================

echo ============================================================ >> lna_final_report.txt
echo FINAL_OUTPUT_FILES >> lna_final_report.txt
echo ============================================================ >> lna_final_report.txt

echo REPORT lna_final_report.txt >> lna_final_report.txt
echo RF_DATA lna_final_target_and_broadband.dat >> lna_final_report.txt
echo RF_RAW lna_final_rf.raw >> lna_final_report.txt
echo STABILITY_DATA lna_final_stability.dat >> lna_final_report.txt
echo STABILITY_RAW lna_final_stability.raw >> lna_final_report.txt

echo ============================================================ >> lna_final_report.txt


* ============================================================================
* TERMINAL SUMMARY
* ============================================================================

echo
echo ============================================================
echo LNA FINAL CHARACTERIZATION SUMMARY
echo ============================================================

echo LNA_TOP_POWER_MW $op_pdc_lna
echo IO_POWER_MW $op_pdc_io
echo TOTAL_POWER_MW $op_pdc_total

echo
echo CENTER_2P4_GHZ
print s11c s21c s12c s22c
print nfc nfminc
print kc muc mupc deltac
print zinrc zinic
print zoutrc zoutic

echo
echo TARGET_BAND_WORST_CASE
print s11max s21min s22max
print nfbandmax
print kbandmin mubandmin mupbandmin deltabandmax
print gain_ripple

echo
echo WIDEBAND_STABILITY_10MHZ_TO_30GHZ
print wbkmin wbmumin wbmupmin wbdeltamax


* ============================================================================
* 4. VISIBLE PLOTS
* ============================================================================


* ---------------------------------------------------------------------------
* Target-band RF plots
* ---------------------------------------------------------------------------

setplot $rfplot
setscale fghz

plot s21db xlimit 2.3 2.5 xlabel 'Frequency (GHz)' ylabel 'S21 Gain (dB)'

plot s11db xlimit 2.3 2.5 xlabel 'Frequency (GHz)' ylabel 'S11 (dB)'

plot s22db xlimit 2.3 2.5 xlabel 'Frequency (GHz)' ylabel 'S22 (dB)'

plot s12db xlimit 2.3 2.5 xlabel 'Frequency (GHz)' ylabel 'S12 Reverse Isolation (dB)'


* Gain + return losses together
plot s21db s11db s22db xlimit 2.3 2.5 xlabel 'Frequency (GHz)' ylabel 'S Parameters (dB)'


* Noise
plot nfdb nfmin_db xlimit 2.3 2.5 xlabel 'Frequency (GHz)' ylabel 'Noise Figure (dB)'


* Stability inside target band
plot mu mup xlimit 2.3 2.5 xlabel 'Frequency (GHz)' ylabel 'Mu Stability Factor'

plot kval xlimit 2.3 2.5 xlabel 'Frequency (GHz)' ylabel 'Rollett K'

plot delta_mag xlimit 2.3 2.5 xlabel 'Frequency (GHz)' ylabel '|Delta|'


* Impedance
plot zin_re zin_im xlimit 2.3 2.5 xlabel 'Frequency (GHz)' ylabel 'Input Impedance (Ohm)'

plot zout_re zout_im xlimit 2.3 2.5 xlabel 'Frequency (GHz)' ylabel 'Output Impedance (Ohm)'


* VSWR
plot vswr_in vswr_out xlimit 2.3 2.5 xlabel 'Frequency (GHz)' ylabel 'VSWR'


* ---------------------------------------------------------------------------
* Broadband response
* ---------------------------------------------------------------------------

plot s21db xlimit 0.01 7 xlabel 'Frequency (GHz)' ylabel 'S21 Gain (dB)'

plot s11db s22db xlimit 0.01 7 xlabel 'Frequency (GHz)' ylabel 'Return Loss (dB)'

plot nfdb nfmin_db xlimit 0.01 7 xlabel 'Frequency (GHz)' ylabel 'Noise Figure (dB)'


* ---------------------------------------------------------------------------
* Very-wide-band stability
* ---------------------------------------------------------------------------

setplot $stabilityplot
setscale wbfghz

plot wbmu wbmup xlimit 0.01 30 xlabel 'Frequency (GHz)' ylabel 'Mu / Mu Prime'

plot wbk xlimit 0.01 30 xlabel 'Frequency (GHz)' ylabel 'Rollett K'

plot wbdelta_mag xlimit 0.01 30 xlabel 'Frequency (GHz)' ylabel '|Delta|'


echo
echo ============================================================
echo FINAL CHARACTERIZATION COMPLETE
echo See: lna_final_report.txt
echo ============================================================

.endc



**** end user architecture code
**.ends
.end
